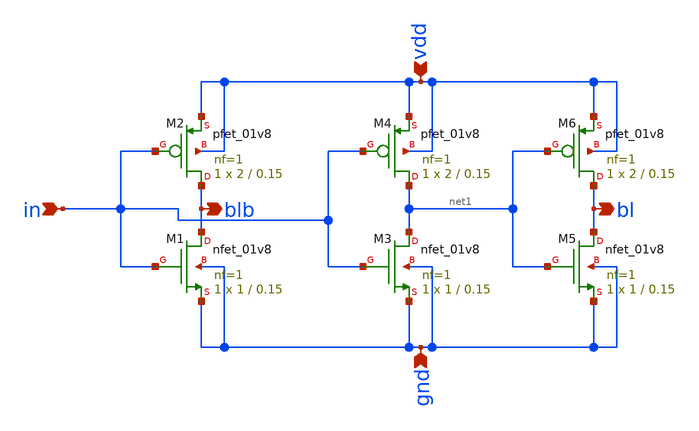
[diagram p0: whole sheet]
** sch_path: Projects/Schematic_Design_and_Analysis_of_an_8-Word_8-Bit_Static_RAM_with_6T_Storage_Cells_using_SKY130PDK/assets/schematic/write_amp.sch
**.subckt write_amp in blb bl vdd gnd
*.ipin in
*.opin blb
*.opin bl
*.ipin vdd
*.ipin gnd
XM1 blb in gnd gnd sky130_fd_pr__nfet_01v8 L=0.15 W=1 nf=1 ad='int((nf+1)/2) * W/nf * 0.29' as='int((nf+2)/2) * W/nf * 0.29'
+ pd='2*int((nf+1)/2) * (W/nf + 0.29)' ps='2*int((nf+2)/2) * (W/nf + 0.29)' nrd='0.29 / W' nrs='0.29 / W'
+ sa=0 sb=0 sd=0 mult=1 m=1
XM2 blb in vdd vdd sky130_fd_pr__pfet_01v8 L=0.15 W=2 nf=1 ad='int((nf+1)/2) * W/nf * 0.29' as='int((nf+2)/2) * W/nf * 0.29'
+ pd='2*int((nf+1)/2) * (W/nf + 0.29)' ps='2*int((nf+2)/2) * (W/nf + 0.29)' nrd='0.29 / W' nrs='0.29 / W'
+ sa=0 sb=0 sd=0 mult=1 m=1
XM3 net1 in gnd gnd sky130_fd_pr__nfet_01v8 L=0.15 W=1 nf=1 ad='int((nf+1)/2) * W/nf * 0.29' as='int((nf+2)/2) * W/nf * 0.29'
+ pd='2*int((nf+1)/2) * (W/nf + 0.29)' ps='2*int((nf+2)/2) * (W/nf + 0.29)' nrd='0.29 / W' nrs='0.29 / W'
+ sa=0 sb=0 sd=0 mult=1 m=1
XM4 net1 in vdd vdd sky130_fd_pr__pfet_01v8 L=0.15 W=2 nf=1 ad='int((nf+1)/2) * W/nf * 0.29' as='int((nf+2)/2) * W/nf * 0.29'
+ pd='2*int((nf+1)/2) * (W/nf + 0.29)' ps='2*int((nf+2)/2) * (W/nf + 0.29)' nrd='0.29 / W' nrs='0.29 / W'
+ sa=0 sb=0 sd=0 mult=1 m=1
XM5 bl net1 gnd gnd sky130_fd_pr__nfet_01v8 L=0.15 W=1 nf=1 ad='int((nf+1)/2) * W/nf * 0.29' as='int((nf+2)/2) * W/nf * 0.29'
+ pd='2*int((nf+1)/2) * (W/nf + 0.29)' ps='2*int((nf+2)/2) * (W/nf + 0.29)' nrd='0.29 / W' nrs='0.29 / W'
+ sa=0 sb=0 sd=0 mult=1 m=1
XM6 bl net1 vdd vdd sky130_fd_pr__pfet_01v8 L=0.15 W=2 nf=1 ad='int((nf+1)/2) * W/nf * 0.29' as='int((nf+2)/2) * W/nf * 0.29'
+ pd='2*int((nf+1)/2) * (W/nf + 0.29)' ps='2*int((nf+2)/2) * (W/nf + 0.29)' nrd='0.29 / W' nrs='0.29 / W'
+ sa=0 sb=0 sd=0 mult=1 m=1
**.ends
.end
